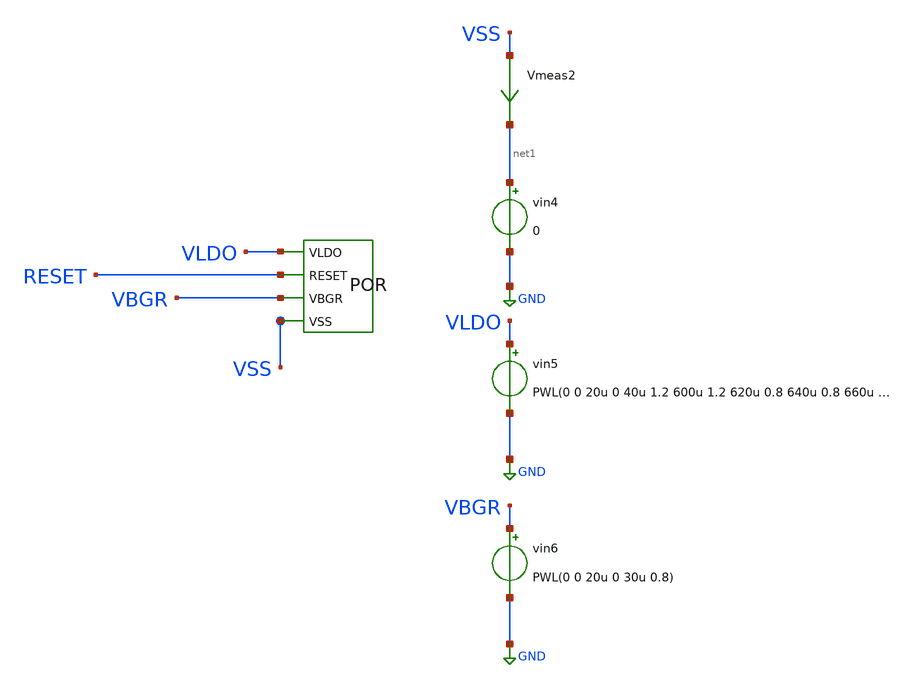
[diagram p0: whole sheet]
** sch_path: dependencies/POR/POR-main/testbenches/corners/xschem/por_post_layout_sim_sf.sch
**.subckt por_post_layout_sim_sf
X1 VLDO RESET VBGR VSS POR
vin4 net1 GND 0
Vmeas2 VSS net1 0
.save i(vmeas2)
vin5 VLDO GND PWL(0 0 20u 0 40u 1.2 600u 1.2 620u 0.8 640u 0.8 660u 1.2 760u 1.2 780u 0)
vin6 VBGR GND PWL(0 0 20u 0 30u 0.8)
**** begin user architecture code



.include /foss/designs/simulations/POR/output/POR__POR/magic_RC/POR.pex.spice
.lib cornerMOSlv.lib mos_sf
.lib cornerMOShv.lib mos_sf
.lib cornerHBT.lib hbt_typ
.lib cornerRES.lib res_typ
.lib cornerDIO.lib dio_tt
.lib cornerCAP.lib cap_typ






.param temp=27
.save all
.control
tran 1u 1m
write por_sf.raw
.endc



**** end user architecture code
**.ends
.GLOBAL GND
.end
